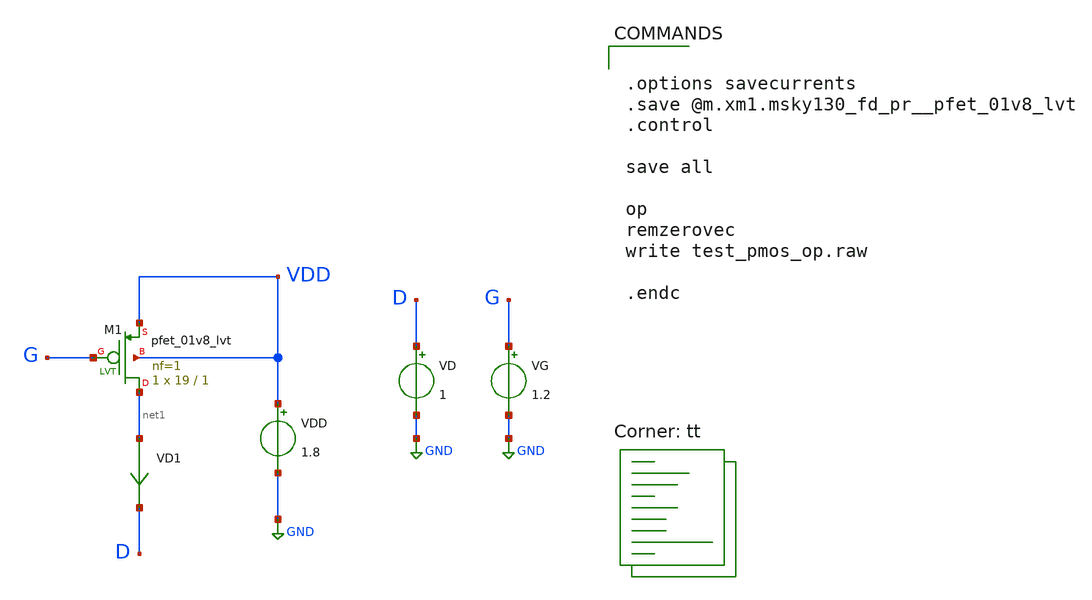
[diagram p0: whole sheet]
** sch_path: strongARM/test_pmos_op.sch
**.subckt test_pmos_op
VG G GND 1.2
VDD VDD GND 1.8
VD1 net1 D 0
.save i(vd1)
VD D GND 1
XM1 net1 G VDD VDD sky130_fd_pr__pfet_01v8_lvt L=1 W=19 nf=1 ad='int((nf+1)/2) * W/nf * 0.29' as='int((nf+2)/2) * W/nf * 0.29'
+ pd='2*int((nf+1)/2) * (W/nf + 0.29)' ps='2*int((nf+2)/2) * (W/nf + 0.29)' nrd='0.29 / W' nrs='0.29 / W'
+ sa=0 sb=0 sd=0 mult=1 m=1
**** begin user architecture code
.lib $::SKYWATER_MODELS/sky130.lib.spice tt


.options savecurrents
.save @m.xm1.msky130_fd_pr__pfet_01v8_lvt
.control

save all

op
remzerovec
write test_pmos_op.raw

.endc


**** end user architecture code
**.ends
.GLOBAL GND
.end
